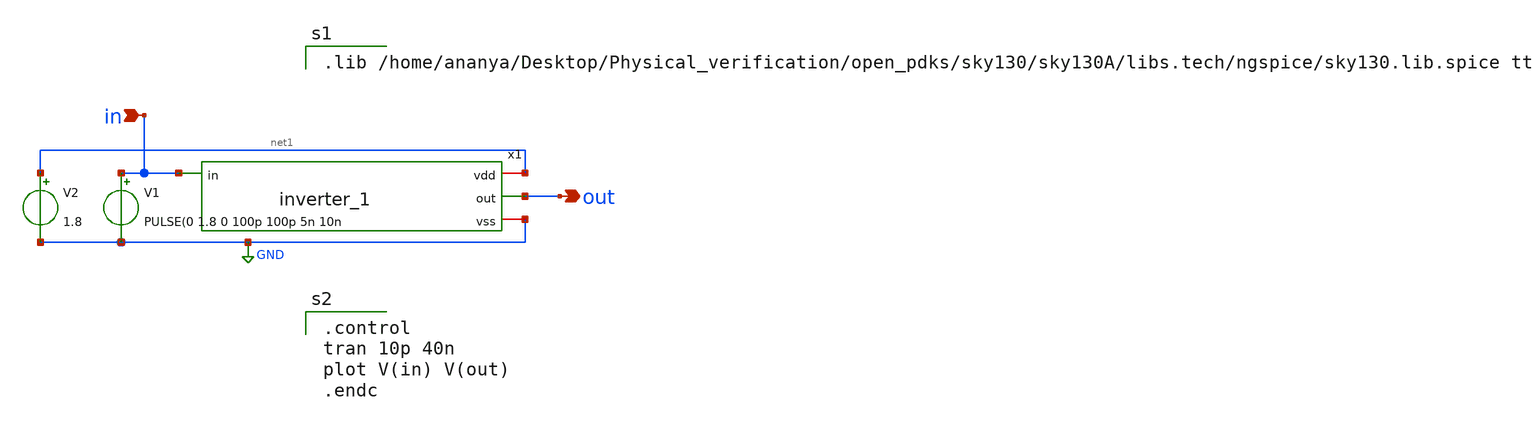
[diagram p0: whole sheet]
** sch_path: Lab1_inverter/xschem/inverter_1_tb.sch
**.subckt inverter_1_tb out in
*.opin out
*.ipin in
x1 net1 in out GND inverter_1
V1 in GND PULSE(0 1.8 0 100p 100p 5n 10n
V2 net1 GND 1.8
**** begin user architecture code

.lib /home/ananya/Desktop/Physical_verification/open_pdks/sky130/sky130A/libs.tech/ngspice/sky130.lib.spice tt


.control
tran 10p 40n
plot V(in) V(out)
.endc

**** end user architecture code
**.ends

* expanding   symbol:  inverter_1.sym # of pins=4
** sym_path: Lab1_inverter/xschem/inverter_1.sym
** sch_path: Lab1_inverter/xschem/inverter_1.sch
.subckt inverter_1 vdd in out vss
*.ipin in
*.opin out
*.iopin vdd
*.iopin vss
XM1 out in vss vss sky130_fd_pr__nfet_01v8 L=0.18 W=4.5 nf=3 ad='int((3 + 1)/2) * 4.5 / 3 * 0.29' as='int((3 + 2)/2) * 4.5 / 3 * 0.29'
+ pd='2*int((3 + 1)/2) * (4.5 / 3 + 0.29)' ps='2*int((3 + 2)/2) * (4.5 / 3 + 0.29)' nrd='0.29 / 4.5 ' nrs='0.29 / 4.5 '
+ sa=0 sb=0 sd=0 mult=1 m=1
XM2 out in vdd vdd sky130_fd_pr__pfet_01v8 L=0.18 W=3 nf=3 ad='int((3 + 1)/2) * 3 / 3 * 0.29' as='int((3 + 2)/2) * 3 / 3 * 0.29'
+ pd='2*int((3 + 1)/2) * (3 / 3 + 0.29)' ps='2*int((3 + 2)/2) * (3 / 3 + 0.29)' nrd='0.29 / 3 ' nrs='0.29 / 3 '
+ sa=0 sb=0 sd=0 mult=1 m=1
.ends

.GLOBAL GND
.end
